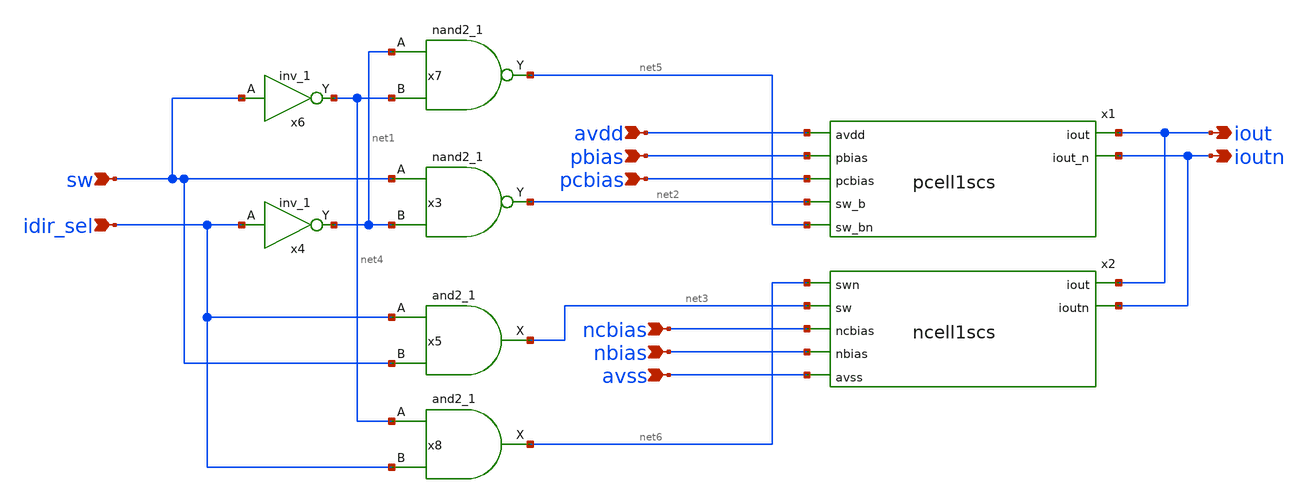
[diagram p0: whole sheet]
** sch_path: xschem/icell1scs.sch
**.subckt icell1scs avdd pbias pcbias sw idir_sel ncbias nbias avss iout ioutn
*.ipin avdd
*.ipin pbias
*.ipin pcbias
*.ipin sw
*.ipin idir_sel
*.ipin ncbias
*.ipin nbias
*.ipin avss
*.opin iout
*.opin ioutn
x3 sw net1 avss avss avdd avdd net2 sky130_fd_sc_hvl__nand2_1
x5 idir_sel sw avss avss avdd avdd net3 sky130_fd_sc_hvl__and2_1
x4 idir_sel avss avss avdd avdd net1 sky130_fd_sc_hvl__inv_1
x6 sw avss avss avdd avdd net4 sky130_fd_sc_hvl__inv_1
x7 net1 net4 avss avss avdd avdd net5 sky130_fd_sc_hvl__nand2_1
x1 avdd pbias pcbias net2 net5 ioutn iout pcell1scs
x2 iout ioutn net6 net3 ncbias nbias avss ncell1scs
x8 net4 idir_sel avss avss avdd avdd net6 sky130_fd_sc_hvl__and2_1
**.ends

* expanding   symbol:  pcell1scs.sym # of pins=7
** sym_path: xschem/pcell1scs.sym
** sch_path: xschem/pcell1scs.sch
.subckt pcell1scs avdd pbias pcbias sw_b sw_bn iout_n iout
*.ipin pbias
*.ipin pcbias
*.ipin sw_b
*.ipin avdd
*.opin iout
*.opin iout_n
*.ipin sw_bn
XM1 net1 pbias avdd avdd sky130_fd_pr__pfet_g5v0d10v5 L=0.5 W=6 nf=1 ad='int((nf+1)/2) * W/nf * 0.29'
+ as='int((nf+2)/2) * W/nf * 0.29' pd='2*int((nf+1)/2) * (W/nf + 0.29)' ps='2*int((nf+2)/2) * (W/nf + 0.29)'
+ nrd='0.29 / W' nrs='0.29 / W' sa=0 sb=0 sd=0 mult=1 m=1
XM2 net2 pcbias net1 avdd sky130_fd_pr__pfet_g5v0d10v5 L=0.5 W=12 nf=1 ad='int((nf+1)/2) * W/nf * 0.29'
+ as='int((nf+2)/2) * W/nf * 0.29' pd='2*int((nf+1)/2) * (W/nf + 0.29)' ps='2*int((nf+2)/2) * (W/nf + 0.29)'
+ nrd='0.29 / W' nrs='0.29 / W' sa=0 sb=0 sd=0 mult=1 m=1
XM3 iout sw_b net2 avdd sky130_fd_pr__pfet_g5v0d10v5 L=0.5 W=4 nf=1 ad='int((nf+1)/2) * W/nf * 0.29'
+ as='int((nf+2)/2) * W/nf * 0.29' pd='2*int((nf+1)/2) * (W/nf + 0.29)' ps='2*int((nf+2)/2) * (W/nf + 0.29)'
+ nrd='0.29 / W' nrs='0.29 / W' sa=0 sb=0 sd=0 mult=1 m=1
XM4 iout_n sw_bn net2 avdd sky130_fd_pr__pfet_g5v0d10v5 L=0.5 W=4 nf=1 ad='int((nf+1)/2) * W/nf * 0.29'
+ as='int((nf+2)/2) * W/nf * 0.29' pd='2*int((nf+1)/2) * (W/nf + 0.29)' ps='2*int((nf+2)/2) * (W/nf + 0.29)'
+ nrd='0.29 / W' nrs='0.29 / W' sa=0 sb=0 sd=0 mult=1 m=1
.ends


* expanding   symbol:  ncell1scs.sym # of pins=7
** sym_path: xschem/ncell1scs.sym
** sch_path: xschem/ncell1scs.sch
.subckt ncell1scs iout ioutn swn sw ncbias nbias avss
*.ipin sw
*.ipin ncbias
*.ipin nbias
*.ipin avss
*.opin iout
*.opin ioutn
*.ipin swn
XM8 net1 nbias avss avss sky130_fd_pr__nfet_g5v0d10v5 L=0.5 W=3 nf=1 ad='int((nf+1)/2) * W/nf * 0.29'
+ as='int((nf+2)/2) * W/nf * 0.29' pd='2*int((nf+1)/2) * (W/nf + 0.29)' ps='2*int((nf+2)/2) * (W/nf + 0.29)'
+ nrd='0.29 / W' nrs='0.29 / W' sa=0 sb=0 sd=0 mult=1 m=1
XM9 net2 ncbias net1 avss sky130_fd_pr__nfet_g5v0d10v5 L=0.5 W=6 nf=1 ad='int((nf+1)/2) * W/nf * 0.29'
+ as='int((nf+2)/2) * W/nf * 0.29' pd='2*int((nf+1)/2) * (W/nf + 0.29)' ps='2*int((nf+2)/2) * (W/nf + 0.29)'
+ nrd='0.29 / W' nrs='0.29 / W' sa=0 sb=0 sd=0 mult=1 m=1
XM1 iout sw net2 avss sky130_fd_pr__nfet_g5v0d10v5 L=0.5 W=6 nf=1 ad='int((nf+1)/2) * W/nf * 0.29' as='int((nf+2)/2) * W/nf * 0.29'
+ pd='2*int((nf+1)/2) * (W/nf + 0.29)' ps='2*int((nf+2)/2) * (W/nf + 0.29)' nrd='0.29 / W' nrs='0.29 / W'
+ sa=0 sb=0 sd=0 mult=1 m=1
XM2 ioutn swn net2 avss sky130_fd_pr__nfet_g5v0d10v5 L=0.5 W=6 nf=1 ad='int((nf+1)/2) * W/nf * 0.29'
+ as='int((nf+2)/2) * W/nf * 0.29' pd='2*int((nf+1)/2) * (W/nf + 0.29)' ps='2*int((nf+2)/2) * (W/nf + 0.29)'
+ nrd='0.29 / W' nrs='0.29 / W' sa=0 sb=0 sd=0 mult=1 m=1
.ends

.end
